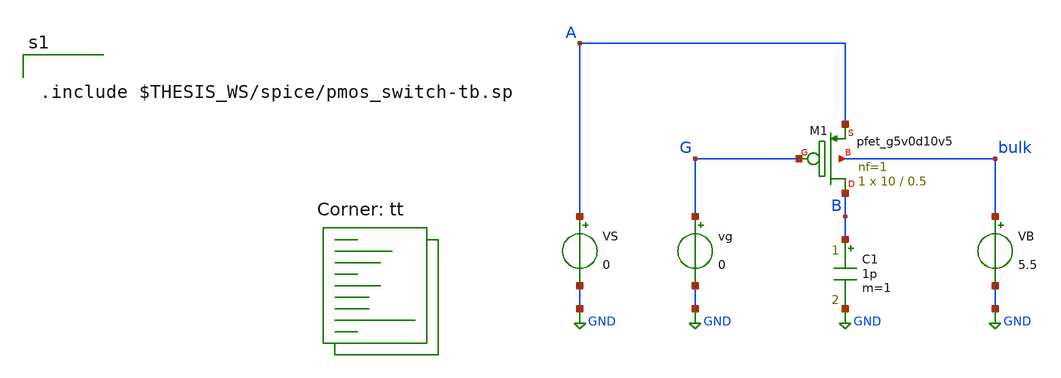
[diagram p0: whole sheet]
** sch_path: xschem/pmos_switch-tb.sch
**.subckt pmos_switch-tb
vg G GND 0
C1 B GND 1p m=1
VS A GND 0
VB bulk GND 5.5
XM1 B G A bulk sky130_fd_pr__pfet_g5v0d10v5 L=0.5 W=10 nf=1 ad='int((nf+1)/2) * W/nf * 0.29' as='int((nf+2)/2) * W/nf * 0.29'
+ pd='2*int((nf+1)/2) * (W/nf + 0.29)' ps='2*int((nf+2)/2) * (W/nf + 0.29)' nrd='0.29 / W' nrs='0.29 / W'
+ sa=0 sb=0 sd=0 mult=1 m=1
**** begin user architecture code
.lib $::SKYWATER_MODELS/sky130.lib.spice tt


.include $THESIS_WS/spice/pmos_switch-tb.sp

**** end user architecture code
**.ends
.GLOBAL GND
.end
